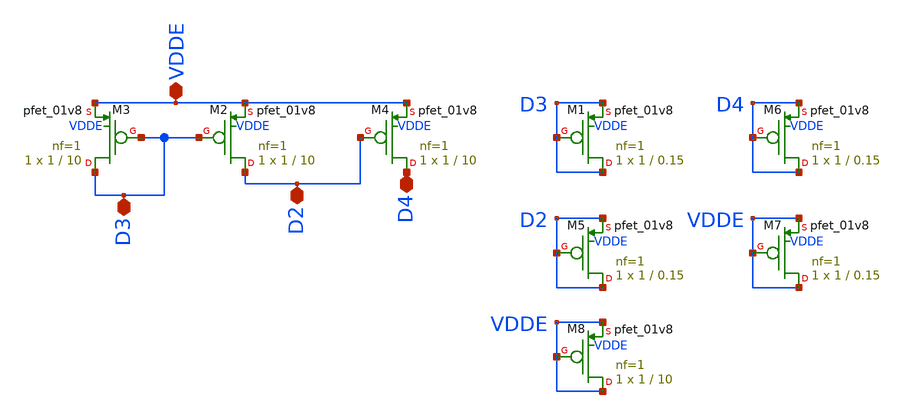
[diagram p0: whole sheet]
** sch_path: magic/pmos_startup.sch
**.subckt pmos_startup VDDE D2 D3 D4
*.iopin VDDE
*.iopin D2
*.iopin D3
*.iopin D4
XM2 D2 D3 VDDE VDDE sky130_fd_pr__pfet_01v8 L=10 W=1 nf=1 ad='int((nf+1)/2) * W/nf * 0.29' as='int((nf+2)/2) * W/nf * 0.29'
+ pd='2*int((nf+1)/2) * (W/nf + 0.29)' ps='2*int((nf+2)/2) * (W/nf + 0.29)' nrd='0.29 / W' nrs='0.29 / W'
+ sa=0 sb=0 sd=0 mult=1 m=1
XM3 D3 D3 VDDE VDDE sky130_fd_pr__pfet_01v8 L=10 W=1 nf=1 ad='int((nf+1)/2) * W/nf * 0.29' as='int((nf+2)/2) * W/nf * 0.29'
+ pd='2*int((nf+1)/2) * (W/nf + 0.29)' ps='2*int((nf+2)/2) * (W/nf + 0.29)' nrd='0.29 / W' nrs='0.29 / W'
+ sa=0 sb=0 sd=0 mult=1 m=1
XM4 D4 D2 VDDE VDDE sky130_fd_pr__pfet_01v8 L=10 W=1 nf=1 ad='int((nf+1)/2) * W/nf * 0.29' as='int((nf+2)/2) * W/nf * 0.29'
+ pd='2*int((nf+1)/2) * (W/nf + 0.29)' ps='2*int((nf+2)/2) * (W/nf + 0.29)' nrd='0.29 / W' nrs='0.29 / W'
+ sa=0 sb=0 sd=0 mult=1 m=1
XM1 D3 D3 D3 VDDE sky130_fd_pr__pfet_01v8 L=0.15 W=1 nf=1 ad='int((nf+1)/2) * W/nf * 0.29' as='int((nf+2)/2) * W/nf * 0.29'
+ pd='2*int((nf+1)/2) * (W/nf + 0.29)' ps='2*int((nf+2)/2) * (W/nf + 0.29)' nrd='0.29 / W' nrs='0.29 / W'
+ sa=0 sb=0 sd=0 mult=1 m=1
XM5 D2 D2 D2 VDDE sky130_fd_pr__pfet_01v8 L=0.15 W=1 nf=1 ad='int((nf+1)/2) * W/nf * 0.29' as='int((nf+2)/2) * W/nf * 0.29'
+ pd='2*int((nf+1)/2) * (W/nf + 0.29)' ps='2*int((nf+2)/2) * (W/nf + 0.29)' nrd='0.29 / W' nrs='0.29 / W'
+ sa=0 sb=0 sd=0 mult=1 m=1
XM6 D4 D4 D4 VDDE sky130_fd_pr__pfet_01v8 L=0.15 W=1 nf=1 ad='int((nf+1)/2) * W/nf * 0.29' as='int((nf+2)/2) * W/nf * 0.29'
+ pd='2*int((nf+1)/2) * (W/nf + 0.29)' ps='2*int((nf+2)/2) * (W/nf + 0.29)' nrd='0.29 / W' nrs='0.29 / W'
+ sa=0 sb=0 sd=0 mult=1 m=1
XM7 VDDE VDDE VDDE VDDE sky130_fd_pr__pfet_01v8 L=0.15 W=1 nf=1 ad='int((nf+1)/2) * W/nf * 0.29' as='int((nf+2)/2) * W/nf * 0.29'
+ pd='2*int((nf+1)/2) * (W/nf + 0.29)' ps='2*int((nf+2)/2) * (W/nf + 0.29)' nrd='0.29 / W' nrs='0.29 / W'
+ sa=0 sb=0 sd=0 mult=1 m=1
XM8 VDDE VDDE VDDE VDDE sky130_fd_pr__pfet_01v8 L=10 W=1 nf=1 ad='int((nf+1)/2) * W/nf * 0.29' as='int((nf+2)/2) * W/nf * 0.29'
+ pd='2*int((nf+1)/2) * (W/nf + 0.29)' ps='2*int((nf+2)/2) * (W/nf + 0.29)' nrd='0.29 / W' nrs='0.29 / W'
+ sa=0 sb=0 sd=0 mult=1 m=1
**.ends
.end
